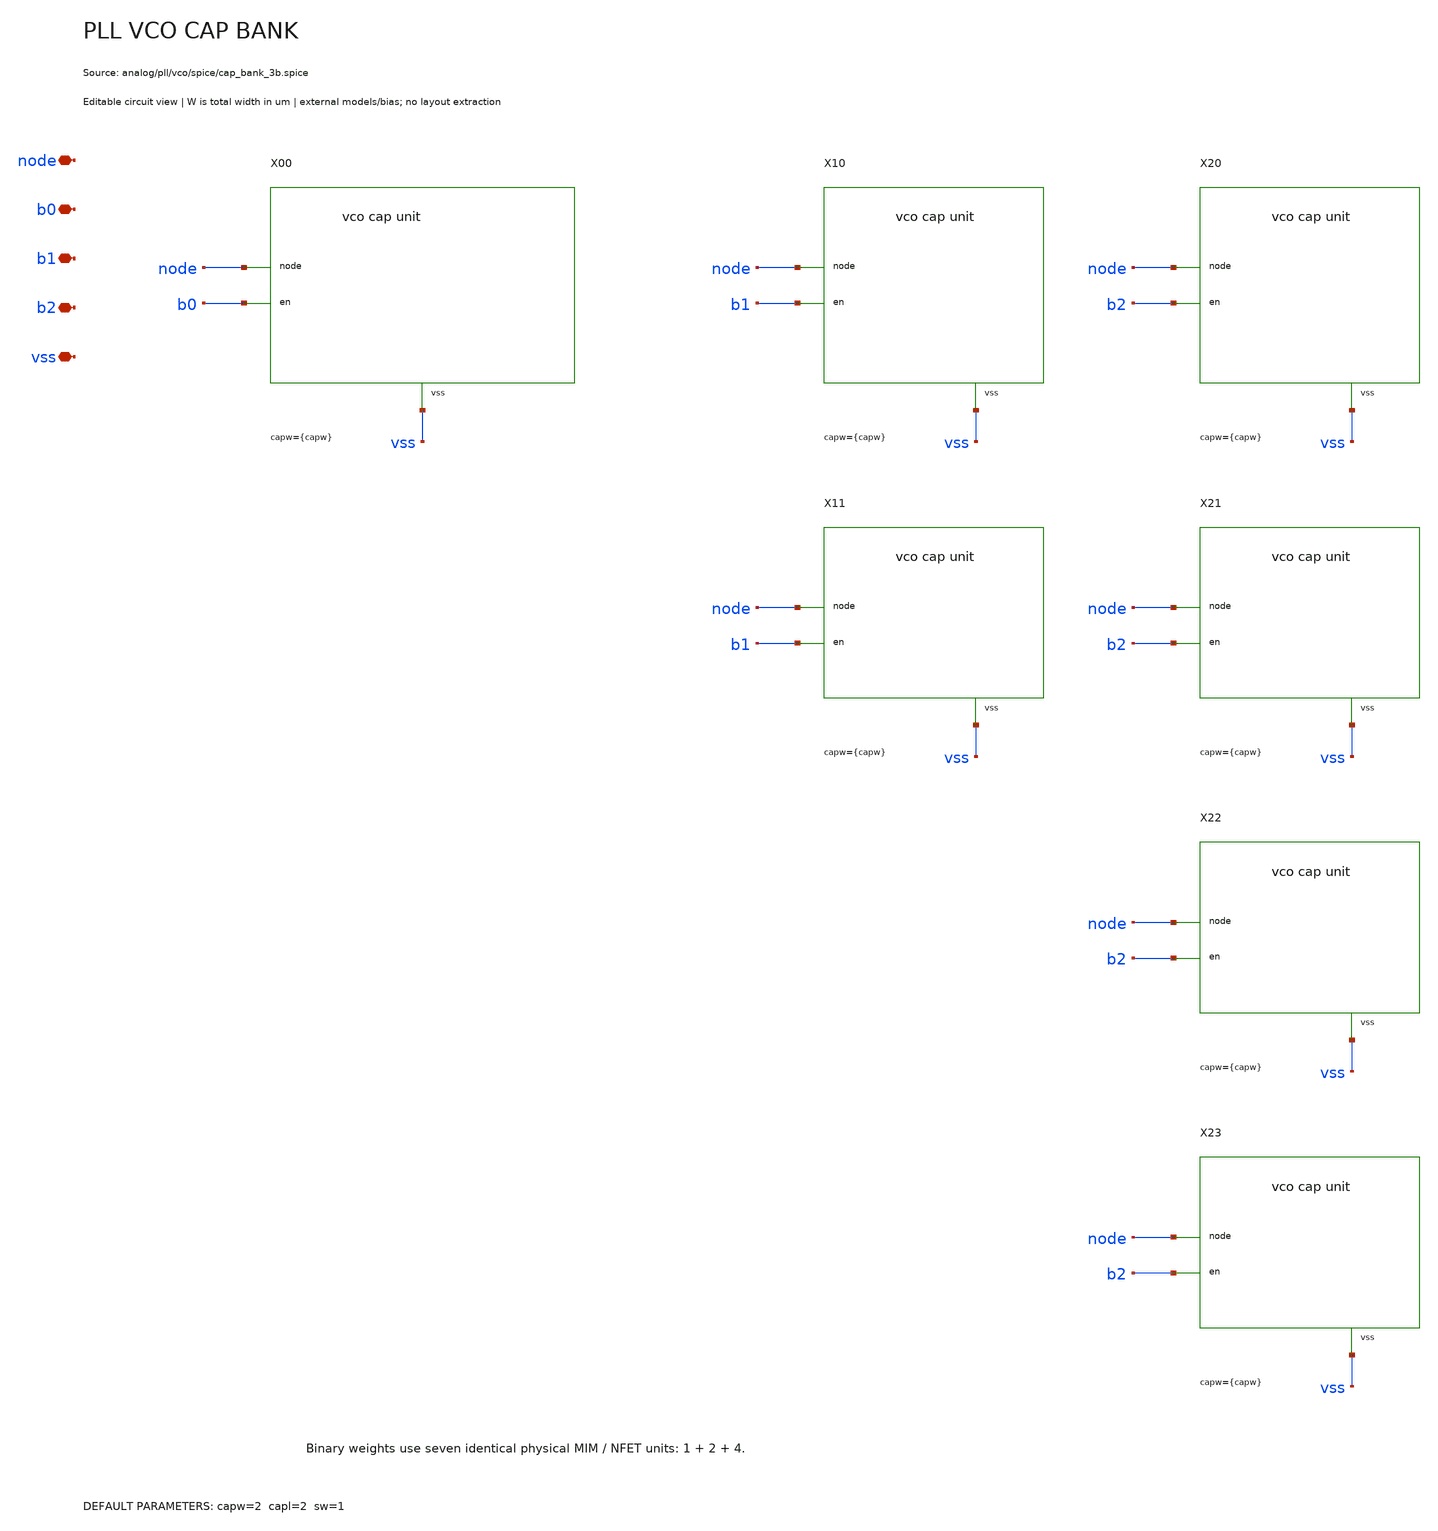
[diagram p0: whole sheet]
** sch_path: analog/pll/vco/schematic/pll_vco_cap_bank.sch
**.subckt pll_vco_cap_bank node b0 b1 b2 vss
*.iopin node
*.iopin b0
*.iopin b1
*.iopin b2
*.iopin vss
X00 node b0 vss pll_vco_cap_unit capw={capw} capl={capl} sw={sw}
X10 node b1 vss pll_vco_cap_unit capw={capw} capl={capl} sw={sw}
X11 node b1 vss pll_vco_cap_unit capw={capw} capl={capl} sw={sw}
X20 node b2 vss pll_vco_cap_unit capw={capw} capl={capl} sw={sw}
X21 node b2 vss pll_vco_cap_unit capw={capw} capl={capl} sw={sw}
X22 node b2 vss pll_vco_cap_unit capw={capw} capl={capl} sw={sw}
X23 node b2 vss pll_vco_cap_unit capw={capw} capl={capl} sw={sw}
**.ends

* expanding   symbol:  serdes/pll_vco_cap_unit.sym # of pins=3
** sym_path: analog/pll/vco/schematic/pll_vco_cap_unit.sym
** sch_path: analog/pll/vco/schematic/pll_vco_cap_unit.sch
.subckt pll_vco_cap_unit node en vss  capw=2 capl=2 sw=1
*.iopin node
*.iopin en
*.iopin vss
Xcap node plate sky130_fd_pr__cap_mim_m3_1 w={capw} l={capl}
Xsw plate en vss vss sky130_fd_pr__nfet_01v8 w={sw} l=0.15 nf=1 ad={sw*0.29} as={sw*0.29} pd={2*(sw+0.29)}
+ ps={2*(sw+0.29)}
Rdc plate vss 1T
.ends

.end
